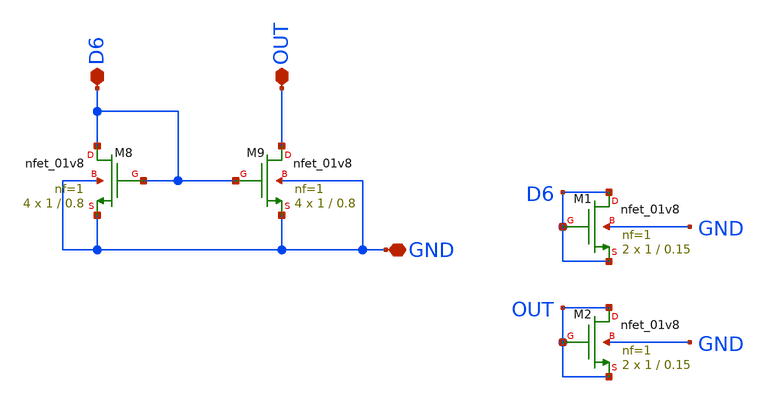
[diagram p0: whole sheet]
** sch_path: opamp/mag/nmos_dif.sch
**.subckt nmos_dif GND D6 OUT
*.iopin GND
*.iopin D6
*.iopin OUT
XM8 D6 D6 GND GND sky130_fd_pr__nfet_01v8 L=0.8 W=1 nf=1 ad='int((nf+1)/2) * W/nf * 0.29' as='int((nf+2)/2) * W/nf * 0.29'
+ pd='2*int((nf+1)/2) * (W/nf + 0.29)' ps='2*int((nf+2)/2) * (W/nf + 0.29)' nrd='0.29 / W' nrs='0.29 / W'
+ sa=0 sb=0 sd=0 mult=4 m=4
XM9 OUT D6 GND GND sky130_fd_pr__nfet_01v8 L=0.8 W=1 nf=1 ad='int((nf+1)/2) * W/nf * 0.29' as='int((nf+2)/2) * W/nf * 0.29'
+ pd='2*int((nf+1)/2) * (W/nf + 0.29)' ps='2*int((nf+2)/2) * (W/nf + 0.29)' nrd='0.29 / W' nrs='0.29 / W'
+ sa=0 sb=0 sd=0 mult=4 m=4
XM1 D6 D6 D6 GND sky130_fd_pr__nfet_01v8 L=0.15 W=1 nf=1 ad='int((nf+1)/2) * W/nf * 0.29' as='int((nf+2)/2) * W/nf * 0.29'
+ pd='2*int((nf+1)/2) * (W/nf + 0.29)' ps='2*int((nf+2)/2) * (W/nf + 0.29)' nrd='0.29 / W' nrs='0.29 / W'
+ sa=0 sb=0 sd=0 mult=2 m=2
XM2 OUT OUT OUT GND sky130_fd_pr__nfet_01v8 L=0.15 W=1 nf=1 ad='int((nf+1)/2) * W/nf * 0.29' as='int((nf+2)/2) * W/nf * 0.29'
+ pd='2*int((nf+1)/2) * (W/nf + 0.29)' ps='2*int((nf+2)/2) * (W/nf + 0.29)' nrd='0.29 / W' nrs='0.29 / W'
+ sa=0 sb=0 sd=0 mult=2 m=2
**.ends
.end
